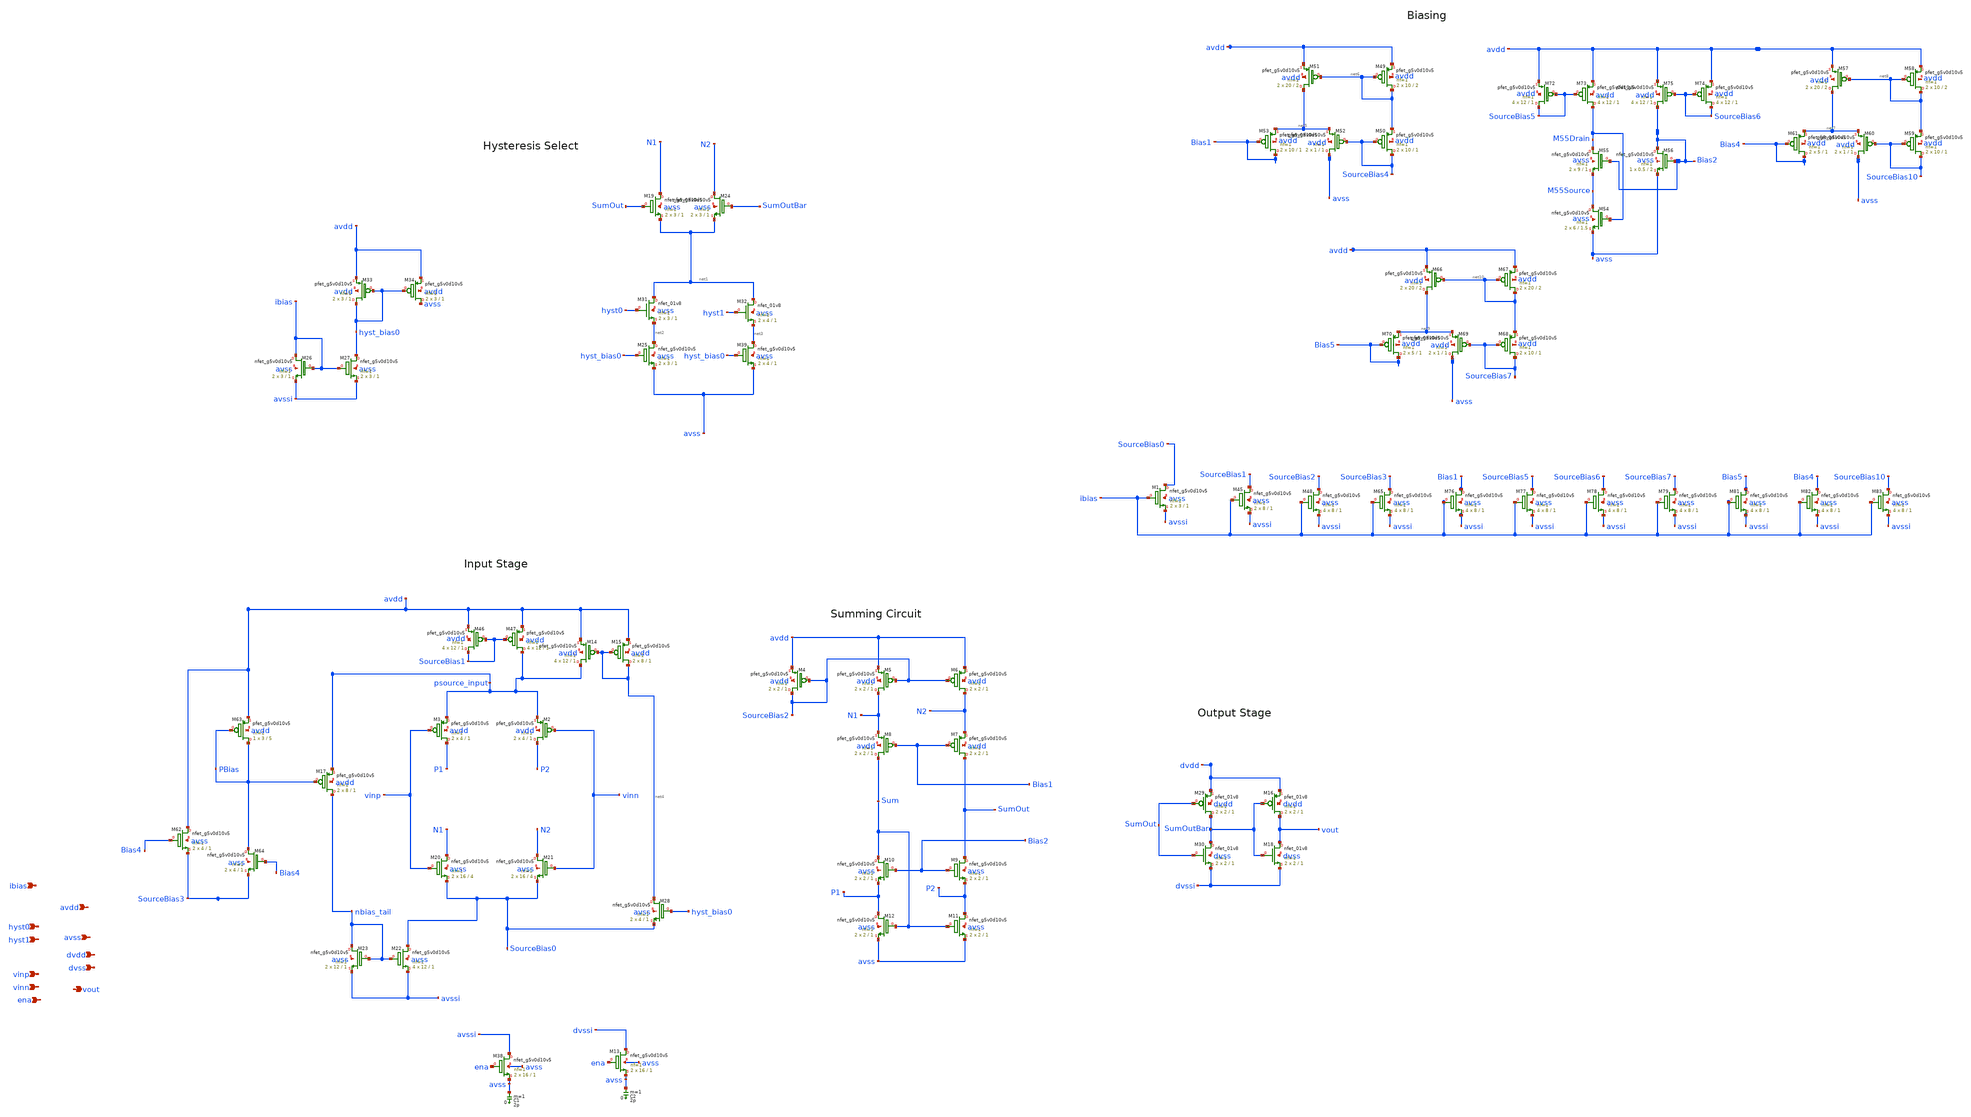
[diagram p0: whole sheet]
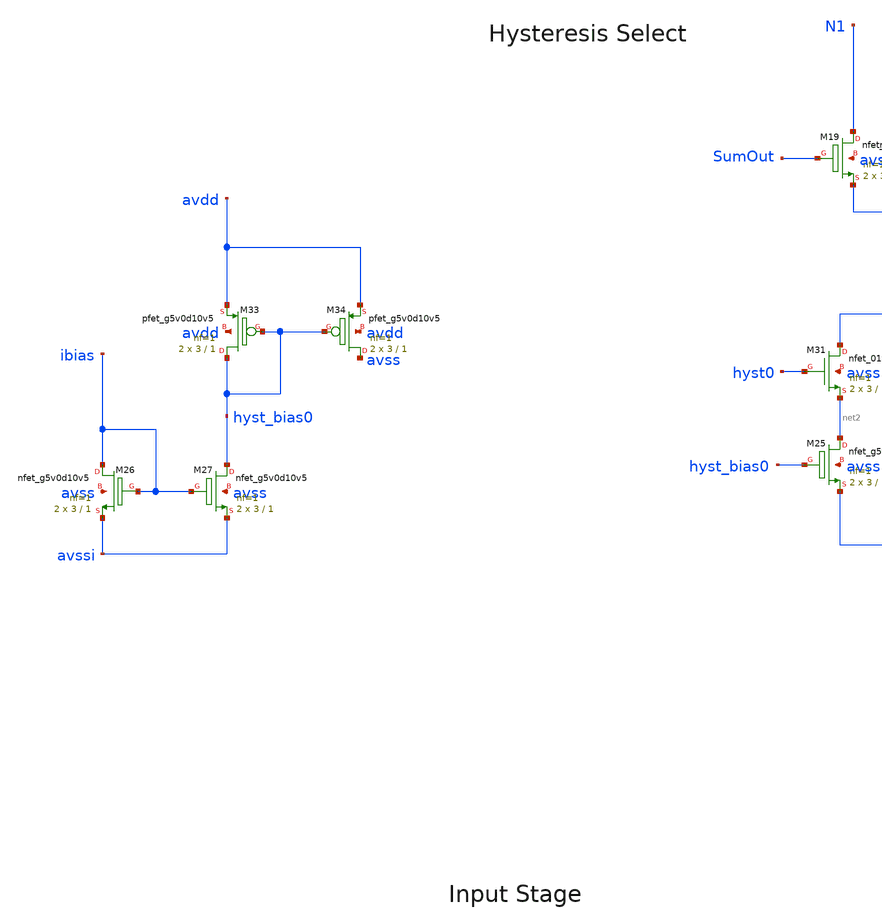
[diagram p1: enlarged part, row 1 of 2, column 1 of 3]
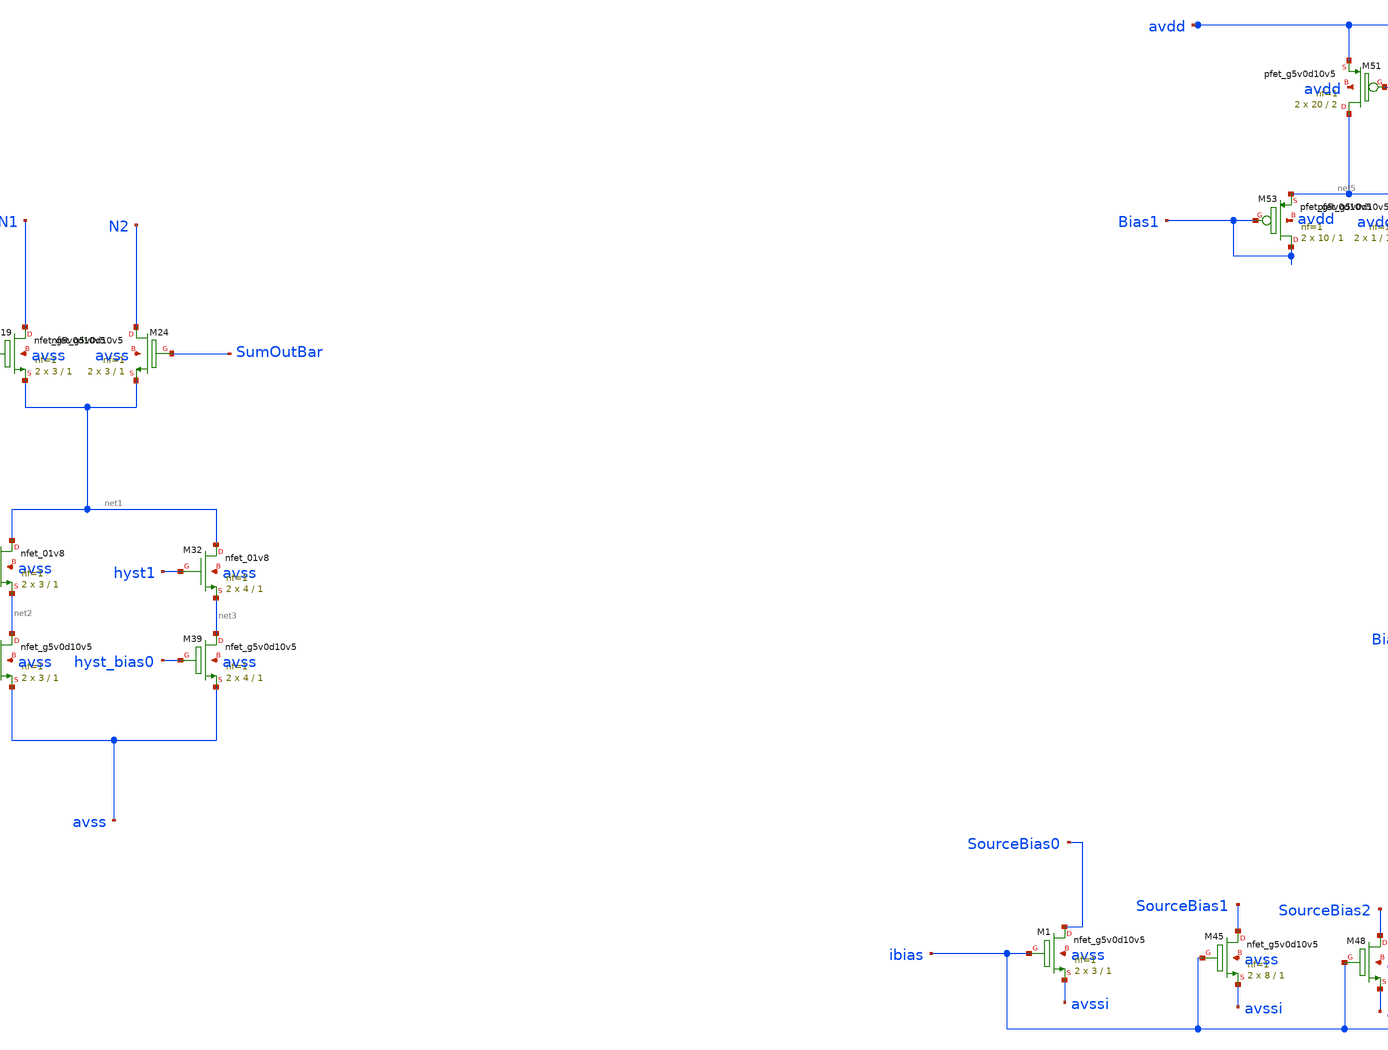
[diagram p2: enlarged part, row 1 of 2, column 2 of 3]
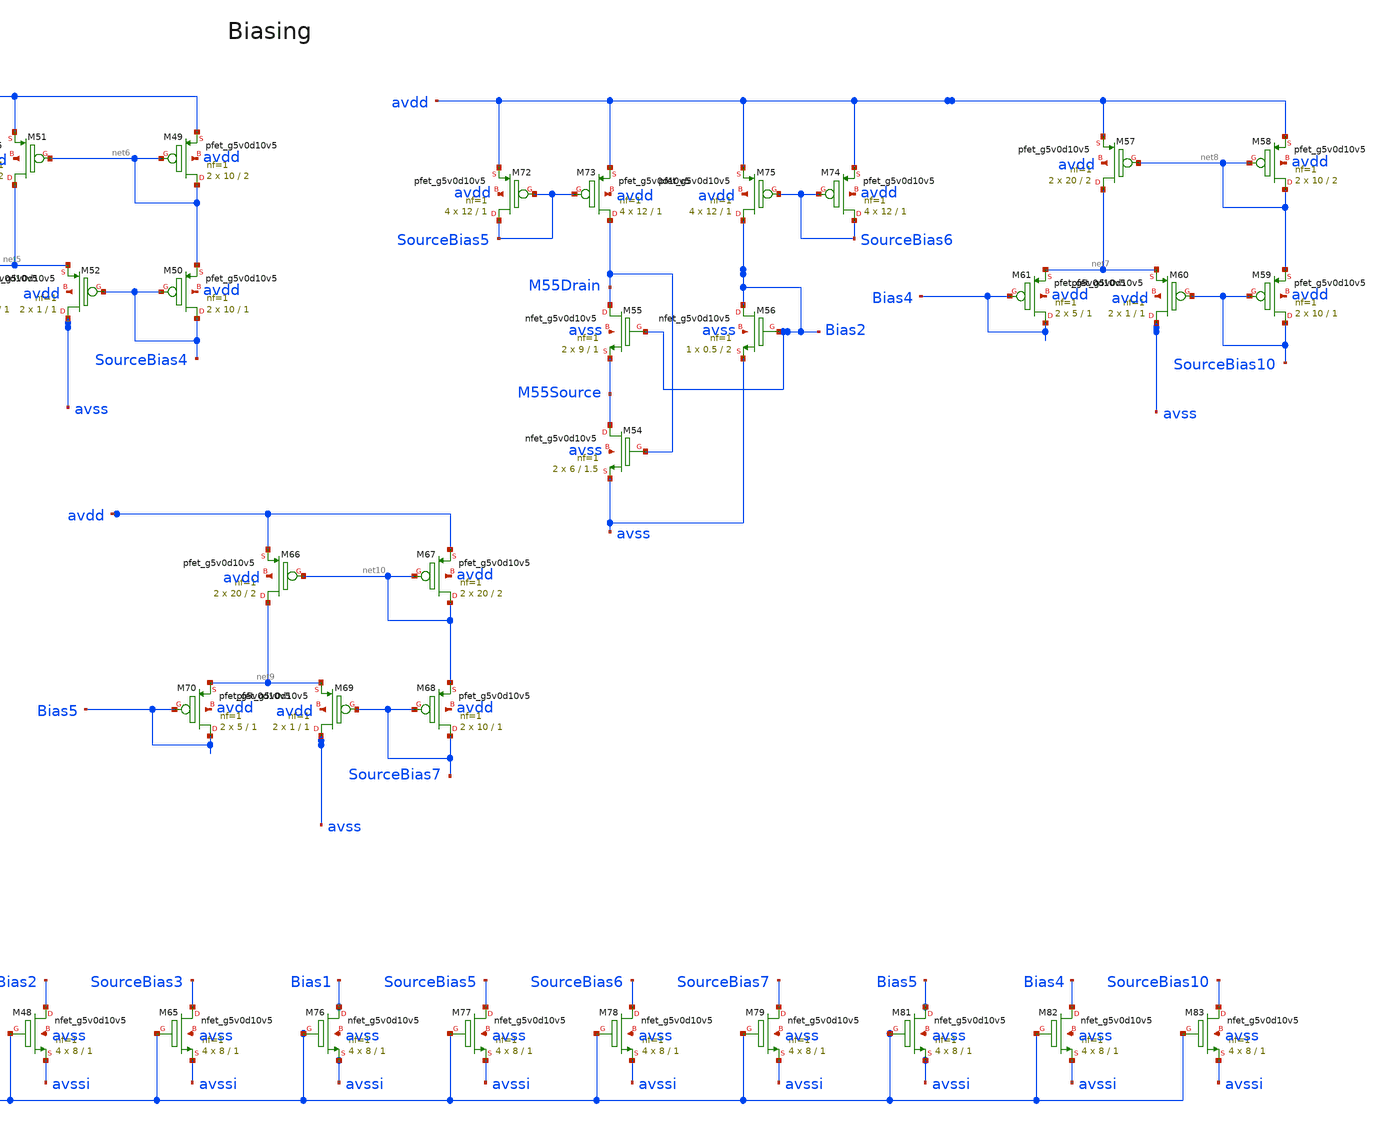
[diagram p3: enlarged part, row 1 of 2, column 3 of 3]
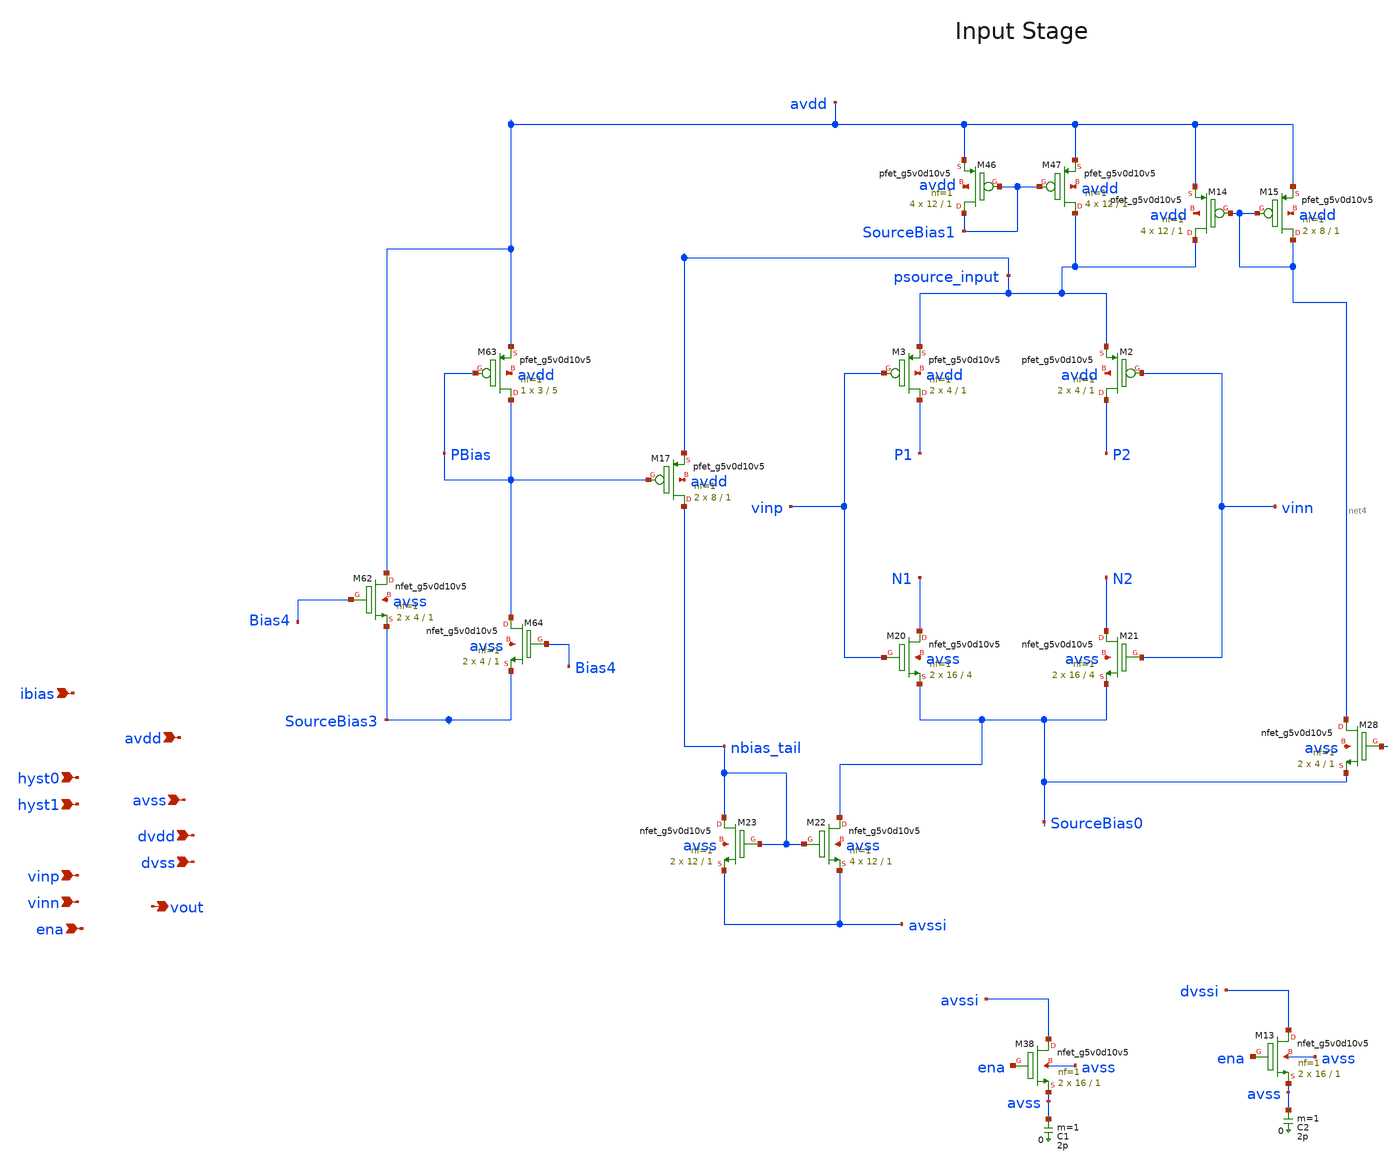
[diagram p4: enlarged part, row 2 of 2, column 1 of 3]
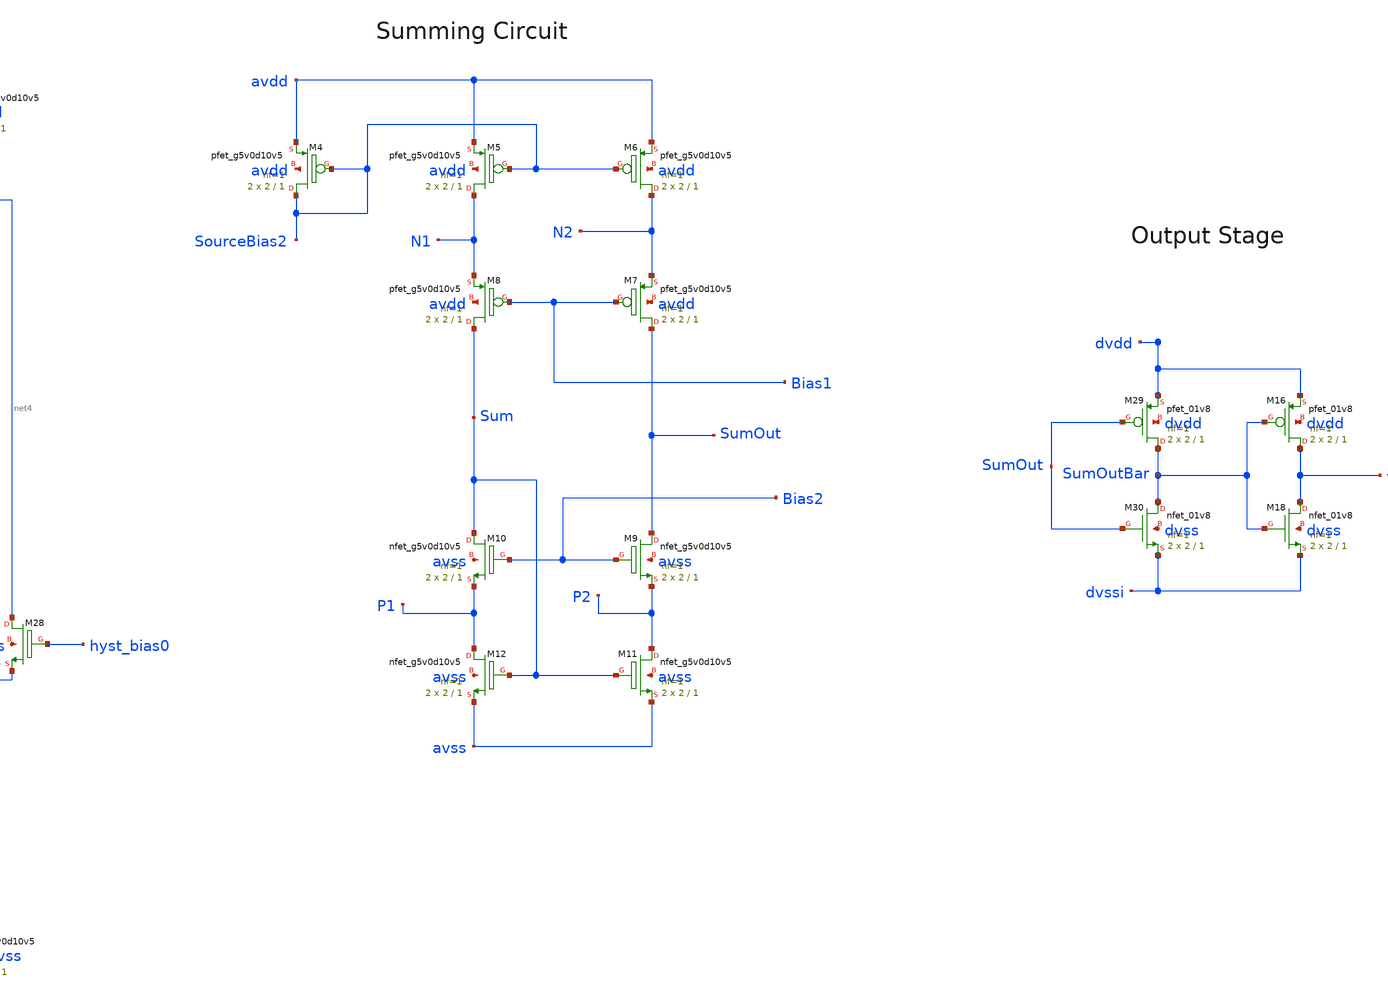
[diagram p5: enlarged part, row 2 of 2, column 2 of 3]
** sch_path: Chipalooza_April2024_Comparator/xschem/Chipalooza_April2024_Comparator.sch
**.subckt Chipalooza_April2024_Comparator vinp vinn hyst0 hyst1 avdd avss dvdd dvss vout ena ibias
*.ipin vinp
*.ipin vinn
*.ipin hyst0
*.ipin hyst1
*.ipin avdd
*.ipin avss
*.ipin dvdd
*.ipin dvss
*.opin vout
*.ipin ena
*.ipin ibias
XM29 SumOutBar SumOut dvdd dvdd sky130_fd_pr__pfet_01v8 L=1 W=2 nf=1 ad='int((nf+1)/2) * W/nf * 0.29'
+ as='int((nf+2)/2) * W/nf * 0.29' pd='2*int((nf+1)/2) * (W/nf + 0.29)' ps='2*int((nf+2)/2) * (W/nf + 0.29)'
+ nrd='0.29 / W' nrs='0.29 / W' sa=0 sb=0 sd=0 mult=2 m=2
XM30 SumOutBar SumOut dvssi dvss sky130_fd_pr__nfet_01v8 L=1 W=2 nf=1 ad='int((nf+1)/2) * W/nf * 0.29'
+ as='int((nf+2)/2) * W/nf * 0.29' pd='2*int((nf+1)/2) * (W/nf + 0.29)' ps='2*int((nf+2)/2) * (W/nf + 0.29)'
+ nrd='0.29 / W' nrs='0.29 / W' sa=0 sb=0 sd=0 mult=2 m=2
XM25 net2 hyst_bias0 avss avss sky130_fd_pr__nfet_g5v0d10v5 L=1 W=3 nf=1 ad='int((nf+1)/2) * W/nf * 0.29'
+ as='int((nf+2)/2) * W/nf * 0.29' pd='2*int((nf+1)/2) * (W/nf + 0.29)' ps='2*int((nf+2)/2) * (W/nf + 0.29)'
+ nrd='0.29 / W' nrs='0.29 / W' sa=0 sb=0 sd=0 mult=2 m=2
C1 avss 0 2p m=1
XM38 avssi ena avss avss sky130_fd_pr__nfet_g5v0d10v5 L=1 W=16 nf=1 ad='int((nf+1)/2) * W/nf * 0.29'
+ as='int((nf+2)/2) * W/nf * 0.29' pd='2*int((nf+1)/2) * (W/nf + 0.29)' ps='2*int((nf+2)/2) * (W/nf + 0.29)'
+ nrd='0.29 / W' nrs='0.29 / W' sa=0 sb=0 sd=0 mult=2 m=2
XM39 net3 hyst_bias0 avss avss sky130_fd_pr__nfet_g5v0d10v5 L=1 W=4 nf=1 ad='int((nf+1)/2) * W/nf * 0.29'
+ as='int((nf+2)/2) * W/nf * 0.29' pd='2*int((nf+1)/2) * (W/nf + 0.29)' ps='2*int((nf+2)/2) * (W/nf + 0.29)'
+ nrd='0.29 / W' nrs='0.29 / W' sa=0 sb=0 sd=0 mult=2 m=2
C2 avss 0 2p m=1
XM13 dvssi ena avss avss sky130_fd_pr__nfet_g5v0d10v5 L=1 W=16 nf=1 ad='int((nf+1)/2) * W/nf * 0.29'
+ as='int((nf+2)/2) * W/nf * 0.29' pd='2*int((nf+1)/2) * (W/nf + 0.29)' ps='2*int((nf+2)/2) * (W/nf + 0.29)'
+ nrd='0.29 / W' nrs='0.29 / W' sa=0 sb=0 sd=0 mult=2 m=2
XM16 vout SumOutBar dvdd dvdd sky130_fd_pr__pfet_01v8 L=1 W=2 nf=1 ad='int((nf+1)/2) * W/nf * 0.29' as='int((nf+2)/2) * W/nf * 0.29'
+ pd='2*int((nf+1)/2) * (W/nf + 0.29)' ps='2*int((nf+2)/2) * (W/nf + 0.29)' nrd='0.29 / W' nrs='0.29 / W'
+ sa=0 sb=0 sd=0 mult=2 m=2
XM18 vout SumOutBar dvssi dvss sky130_fd_pr__nfet_01v8 L=1 W=2 nf=1 ad='int((nf+1)/2) * W/nf * 0.29'
+ as='int((nf+2)/2) * W/nf * 0.29' pd='2*int((nf+1)/2) * (W/nf + 0.29)' ps='2*int((nf+2)/2) * (W/nf + 0.29)'
+ nrd='0.29 / W' nrs='0.29 / W' sa=0 sb=0 sd=0 mult=2 m=2
XM4 SourceBias2 SourceBias2 avdd avdd sky130_fd_pr__pfet_g5v0d10v5 L=1 W=2 nf=1 ad='int((nf+1)/2) * W/nf * 0.29'
+ as='int((nf+2)/2) * W/nf * 0.29' pd='2*int((nf+1)/2) * (W/nf + 0.29)' ps='2*int((nf+2)/2) * (W/nf + 0.29)'
+ nrd='0.29 / W' nrs='0.29 / W' sa=0 sb=0 sd=0 mult=2 m=2
XM5 N1 SourceBias2 avdd avdd sky130_fd_pr__pfet_g5v0d10v5 L=1 W=2 nf=1 ad='int((nf+1)/2) * W/nf * 0.29'
+ as='int((nf+2)/2) * W/nf * 0.29' pd='2*int((nf+1)/2) * (W/nf + 0.29)' ps='2*int((nf+2)/2) * (W/nf + 0.29)'
+ nrd='0.29 / W' nrs='0.29 / W' sa=0 sb=0 sd=0 mult=2 m=2
XM6 N2 SourceBias2 avdd avdd sky130_fd_pr__pfet_g5v0d10v5 L=1 W=2 nf=1 ad='int((nf+1)/2) * W/nf * 0.29'
+ as='int((nf+2)/2) * W/nf * 0.29' pd='2*int((nf+1)/2) * (W/nf + 0.29)' ps='2*int((nf+2)/2) * (W/nf + 0.29)'
+ nrd='0.29 / W' nrs='0.29 / W' sa=0 sb=0 sd=0 mult=2 m=2
XM7 SumOut Bias1 N2 avdd sky130_fd_pr__pfet_g5v0d10v5 L=1 W=2 nf=1 ad='int((nf+1)/2) * W/nf * 0.29' as='int((nf+2)/2) * W/nf * 0.29'
+ pd='2*int((nf+1)/2) * (W/nf + 0.29)' ps='2*int((nf+2)/2) * (W/nf + 0.29)' nrd='0.29 / W' nrs='0.29 / W'
+ sa=0 sb=0 sd=0 mult=2 m=2
XM8 Sum Bias1 N1 avdd sky130_fd_pr__pfet_g5v0d10v5 L=1 W=2 nf=1 ad='int((nf+1)/2) * W/nf * 0.29' as='int((nf+2)/2) * W/nf * 0.29'
+ pd='2*int((nf+1)/2) * (W/nf + 0.29)' ps='2*int((nf+2)/2) * (W/nf + 0.29)' nrd='0.29 / W' nrs='0.29 / W'
+ sa=0 sb=0 sd=0 mult=2 m=2
XM9 SumOut Bias2 P2 avss sky130_fd_pr__nfet_g5v0d10v5 L=1 W=2 nf=1 ad='int((nf+1)/2) * W/nf * 0.29' as='int((nf+2)/2) * W/nf * 0.29'
+ pd='2*int((nf+1)/2) * (W/nf + 0.29)' ps='2*int((nf+2)/2) * (W/nf + 0.29)' nrd='0.29 / W' nrs='0.29 / W'
+ sa=0 sb=0 sd=0 mult=2 m=2
XM10 Sum Bias2 P1 avss sky130_fd_pr__nfet_g5v0d10v5 L=1 W=2 nf=1 ad='int((nf+1)/2) * W/nf * 0.29' as='int((nf+2)/2) * W/nf * 0.29'
+ pd='2*int((nf+1)/2) * (W/nf + 0.29)' ps='2*int((nf+2)/2) * (W/nf + 0.29)' nrd='0.29 / W' nrs='0.29 / W'
+ sa=0 sb=0 sd=0 mult=2 m=2
XM11 P2 Sum avss avss sky130_fd_pr__nfet_g5v0d10v5 L=1 W=2 nf=1 ad='int((nf+1)/2) * W/nf * 0.29' as='int((nf+2)/2) * W/nf * 0.29'
+ pd='2*int((nf+1)/2) * (W/nf + 0.29)' ps='2*int((nf+2)/2) * (W/nf + 0.29)' nrd='0.29 / W' nrs='0.29 / W'
+ sa=0 sb=0 sd=0 mult=2 m=2
XM12 P1 Sum avss avss sky130_fd_pr__nfet_g5v0d10v5 L=1 W=2 nf=1 ad='int((nf+1)/2) * W/nf * 0.29' as='int((nf+2)/2) * W/nf * 0.29'
+ pd='2*int((nf+1)/2) * (W/nf + 0.29)' ps='2*int((nf+2)/2) * (W/nf + 0.29)' nrd='0.29 / W' nrs='0.29 / W'
+ sa=0 sb=0 sd=0 mult=2 m=2
XM2 P2 vinn psource_input avdd sky130_fd_pr__pfet_g5v0d10v5 L=1 W=4 nf=1 ad='int((nf+1)/2) * W/nf * 0.29'
+ as='int((nf+2)/2) * W/nf * 0.29' pd='2*int((nf+1)/2) * (W/nf + 0.29)' ps='2*int((nf+2)/2) * (W/nf + 0.29)'
+ nrd='0.29 / W' nrs='0.29 / W' sa=0 sb=0 sd=0 mult=2 m=2
XM3 P1 vinp psource_input avdd sky130_fd_pr__pfet_g5v0d10v5 L=1 W=4 nf=1 ad='int((nf+1)/2) * W/nf * 0.29'
+ as='int((nf+2)/2) * W/nf * 0.29' pd='2*int((nf+1)/2) * (W/nf + 0.29)' ps='2*int((nf+2)/2) * (W/nf + 0.29)'
+ nrd='0.29 / W' nrs='0.29 / W' sa=0 sb=0 sd=0 mult=2 m=2
XM14 psource_input net4 avdd avdd sky130_fd_pr__pfet_g5v0d10v5 L=1 W=12 nf=1 ad='int((nf+1)/2) * W/nf * 0.29'
+ as='int((nf+2)/2) * W/nf * 0.29' pd='2*int((nf+1)/2) * (W/nf + 0.29)' ps='2*int((nf+2)/2) * (W/nf + 0.29)'
+ nrd='0.29 / W' nrs='0.29 / W' sa=0 sb=0 sd=0 mult=4 m=4
XM15 net4 net4 avdd avdd sky130_fd_pr__pfet_g5v0d10v5 L=1 W=8 nf=1 ad='int((nf+1)/2) * W/nf * 0.29' as='int((nf+2)/2) * W/nf * 0.29'
+ pd='2*int((nf+1)/2) * (W/nf + 0.29)' ps='2*int((nf+2)/2) * (W/nf + 0.29)' nrd='0.29 / W' nrs='0.29 / W'
+ sa=0 sb=0 sd=0 mult=2 m=2
XM17 nbias_tail PBias psource_input avdd sky130_fd_pr__pfet_g5v0d10v5 L=1 W=8 nf=1 ad='int((nf+1)/2) * W/nf * 0.29'
+ as='int((nf+2)/2) * W/nf * 0.29' pd='2*int((nf+1)/2) * (W/nf + 0.29)' ps='2*int((nf+2)/2) * (W/nf + 0.29)'
+ nrd='0.29 / W' nrs='0.29 / W' sa=0 sb=0 sd=0 mult=2 m=2
XM20 N1 vinp SourceBias0 avss sky130_fd_pr__nfet_g5v0d10v5 L=4 W=16 nf=1 ad='int((nf+1)/2) * W/nf * 0.29'
+ as='int((nf+2)/2) * W/nf * 0.29' pd='2*int((nf+1)/2) * (W/nf + 0.29)' ps='2*int((nf+2)/2) * (W/nf + 0.29)'
+ nrd='0.29 / W' nrs='0.29 / W' sa=0 sb=0 sd=0 mult=2 m=2
XM21 N2 vinn SourceBias0 avss sky130_fd_pr__nfet_g5v0d10v5 L=4 W=16 nf=1 ad='int((nf+1)/2) * W/nf * 0.29'
+ as='int((nf+2)/2) * W/nf * 0.29' pd='2*int((nf+1)/2) * (W/nf + 0.29)' ps='2*int((nf+2)/2) * (W/nf + 0.29)'
+ nrd='0.29 / W' nrs='0.29 / W' sa=0 sb=0 sd=0 mult=2 m=2
XM22 SourceBias0 nbias_tail avssi avss sky130_fd_pr__nfet_g5v0d10v5 L=1 W=12 nf=1 ad='int((nf+1)/2) * W/nf * 0.29'
+ as='int((nf+2)/2) * W/nf * 0.29' pd='2*int((nf+1)/2) * (W/nf + 0.29)' ps='2*int((nf+2)/2) * (W/nf + 0.29)'
+ nrd='0.29 / W' nrs='0.29 / W' sa=0 sb=0 sd=0 mult=4 m=4
XM23 nbias_tail nbias_tail avssi avss sky130_fd_pr__nfet_g5v0d10v5 L=1 W=12 nf=1 ad='int((nf+1)/2) * W/nf * 0.29'
+ as='int((nf+2)/2) * W/nf * 0.29' pd='2*int((nf+1)/2) * (W/nf + 0.29)' ps='2*int((nf+2)/2) * (W/nf + 0.29)'
+ nrd='0.29 / W' nrs='0.29 / W' sa=0 sb=0 sd=0 mult=2 m=2
XM28 net4 hyst_bias0 SourceBias0 avss sky130_fd_pr__nfet_g5v0d10v5 L=1 W=4 nf=1 ad='int((nf+1)/2) * W/nf * 0.29'
+ as='int((nf+2)/2) * W/nf * 0.29' pd='2*int((nf+1)/2) * (W/nf + 0.29)' ps='2*int((nf+2)/2) * (W/nf + 0.29)'
+ nrd='0.29 / W' nrs='0.29 / W' sa=0 sb=0 sd=0 mult=2 m=2
XM45 SourceBias1 ibias avssi avss sky130_fd_pr__nfet_g5v0d10v5 L=1 W=8 nf=1 ad='int((nf+1)/2) * W/nf * 0.29'
+ as='int((nf+2)/2) * W/nf * 0.29' pd='2*int((nf+1)/2) * (W/nf + 0.29)' ps='2*int((nf+2)/2) * (W/nf + 0.29)'
+ nrd='0.29 / W' nrs='0.29 / W' sa=0 sb=0 sd=0 mult=2 m=2
XM46 SourceBias1 SourceBias1 avdd avdd sky130_fd_pr__pfet_g5v0d10v5 L=1 W=12 nf=1 ad='int((nf+1)/2) * W/nf * 0.29'
+ as='int((nf+2)/2) * W/nf * 0.29' pd='2*int((nf+1)/2) * (W/nf + 0.29)' ps='2*int((nf+2)/2) * (W/nf + 0.29)'
+ nrd='0.29 / W' nrs='0.29 / W' sa=0 sb=0 sd=0 mult=4 m=4
XM47 psource_input SourceBias1 avdd avdd sky130_fd_pr__pfet_g5v0d10v5 L=1 W=12 nf=1 ad='int((nf+1)/2) * W/nf * 0.29'
+ as='int((nf+2)/2) * W/nf * 0.29' pd='2*int((nf+1)/2) * (W/nf + 0.29)' ps='2*int((nf+2)/2) * (W/nf + 0.29)'
+ nrd='0.29 / W' nrs='0.29 / W' sa=0 sb=0 sd=0 mult=4 m=4
XM48 SourceBias2 ibias avssi avss sky130_fd_pr__nfet_g5v0d10v5 L=1 W=8 nf=1 ad='int((nf+1)/2) * W/nf * 0.29'
+ as='int((nf+2)/2) * W/nf * 0.29' pd='2*int((nf+1)/2) * (W/nf + 0.29)' ps='2*int((nf+2)/2) * (W/nf + 0.29)'
+ nrd='0.29 / W' nrs='0.29 / W' sa=0 sb=0 sd=0 mult=4 m=4
XM63 PBias PBias avdd avdd sky130_fd_pr__pfet_g5v0d10v5 L=5 W=3 nf=1 ad='int((nf+1)/2) * W/nf * 0.29'
+ as='int((nf+2)/2) * W/nf * 0.29' pd='2*int((nf+1)/2) * (W/nf + 0.29)' ps='2*int((nf+2)/2) * (W/nf + 0.29)'
+ nrd='0.29 / W' nrs='0.29 / W' sa=0 sb=0 sd=0 mult=1 m=1
XM62 avdd Bias4 SourceBias3 avss sky130_fd_pr__nfet_g5v0d10v5 L=1 W=4 nf=1 ad='int((nf+1)/2) * W/nf * 0.29'
+ as='int((nf+2)/2) * W/nf * 0.29' pd='2*int((nf+1)/2) * (W/nf + 0.29)' ps='2*int((nf+2)/2) * (W/nf + 0.29)'
+ nrd='0.29 / W' nrs='0.29 / W' sa=0 sb=0 sd=0 mult=2 m=2
XM64 PBias Bias4 SourceBias3 avss sky130_fd_pr__nfet_g5v0d10v5 L=1 W=4 nf=1 ad='int((nf+1)/2) * W/nf * 0.29'
+ as='int((nf+2)/2) * W/nf * 0.29' pd='2*int((nf+1)/2) * (W/nf + 0.29)' ps='2*int((nf+2)/2) * (W/nf + 0.29)'
+ nrd='0.29 / W' nrs='0.29 / W' sa=0 sb=0 sd=0 mult=2 m=2
XM65 SourceBias3 ibias avssi avss sky130_fd_pr__nfet_g5v0d10v5 L=1 W=8 nf=1 ad='int((nf+1)/2) * W/nf * 0.29'
+ as='int((nf+2)/2) * W/nf * 0.29' pd='2*int((nf+1)/2) * (W/nf + 0.29)' ps='2*int((nf+2)/2) * (W/nf + 0.29)'
+ nrd='0.29 / W' nrs='0.29 / W' sa=0 sb=0 sd=0 mult=4 m=4
XM76 Bias1 ibias avssi avss sky130_fd_pr__nfet_g5v0d10v5 L=1 W=8 nf=1 ad='int((nf+1)/2) * W/nf * 0.29'
+ as='int((nf+2)/2) * W/nf * 0.29' pd='2*int((nf+1)/2) * (W/nf + 0.29)' ps='2*int((nf+2)/2) * (W/nf + 0.29)'
+ nrd='0.29 / W' nrs='0.29 / W' sa=0 sb=0 sd=0 mult=4 m=4
XM77 SourceBias5 ibias avssi avss sky130_fd_pr__nfet_g5v0d10v5 L=1 W=8 nf=1 ad='int((nf+1)/2) * W/nf * 0.29'
+ as='int((nf+2)/2) * W/nf * 0.29' pd='2*int((nf+1)/2) * (W/nf + 0.29)' ps='2*int((nf+2)/2) * (W/nf + 0.29)'
+ nrd='0.29 / W' nrs='0.29 / W' sa=0 sb=0 sd=0 mult=4 m=4
XM78 SourceBias6 ibias avssi avss sky130_fd_pr__nfet_g5v0d10v5 L=1 W=8 nf=1 ad='int((nf+1)/2) * W/nf * 0.29'
+ as='int((nf+2)/2) * W/nf * 0.29' pd='2*int((nf+1)/2) * (W/nf + 0.29)' ps='2*int((nf+2)/2) * (W/nf + 0.29)'
+ nrd='0.29 / W' nrs='0.29 / W' sa=0 sb=0 sd=0 mult=4 m=4
XM79 SourceBias7 ibias avssi avss sky130_fd_pr__nfet_g5v0d10v5 L=1 W=8 nf=1 ad='int((nf+1)/2) * W/nf * 0.29'
+ as='int((nf+2)/2) * W/nf * 0.29' pd='2*int((nf+1)/2) * (W/nf + 0.29)' ps='2*int((nf+2)/2) * (W/nf + 0.29)'
+ nrd='0.29 / W' nrs='0.29 / W' sa=0 sb=0 sd=0 mult=4 m=4
XM81 Bias5 ibias avssi avss sky130_fd_pr__nfet_g5v0d10v5 L=1 W=8 nf=1 ad='int((nf+1)/2) * W/nf * 0.29'
+ as='int((nf+2)/2) * W/nf * 0.29' pd='2*int((nf+1)/2) * (W/nf + 0.29)' ps='2*int((nf+2)/2) * (W/nf + 0.29)'
+ nrd='0.29 / W' nrs='0.29 / W' sa=0 sb=0 sd=0 mult=4 m=4
XM82 Bias4 ibias avssi avss sky130_fd_pr__nfet_g5v0d10v5 L=1 W=8 nf=1 ad='int((nf+1)/2) * W/nf * 0.29'
+ as='int((nf+2)/2) * W/nf * 0.29' pd='2*int((nf+1)/2) * (W/nf + 0.29)' ps='2*int((nf+2)/2) * (W/nf + 0.29)'
+ nrd='0.29 / W' nrs='0.29 / W' sa=0 sb=0 sd=0 mult=4 m=4
XM83 SourceBias10 ibias avssi avss sky130_fd_pr__nfet_g5v0d10v5 L=1 W=8 nf=1 ad='int((nf+1)/2) * W/nf * 0.29'
+ as='int((nf+2)/2) * W/nf * 0.29' pd='2*int((nf+1)/2) * (W/nf + 0.29)' ps='2*int((nf+2)/2) * (W/nf + 0.29)'
+ nrd='0.29 / W' nrs='0.29 / W' sa=0 sb=0 sd=0 mult=4 m=4
XM54 M55Source M55Drain avss avss sky130_fd_pr__nfet_g5v0d10v5 L=1.5 W=6 nf=1 ad='int((nf+1)/2) * W/nf * 0.29'
+ as='int((nf+2)/2) * W/nf * 0.29' pd='2*int((nf+1)/2) * (W/nf + 0.29)' ps='2*int((nf+2)/2) * (W/nf + 0.29)'
+ nrd='0.29 / W' nrs='0.29 / W' sa=0 sb=0 sd=0 mult=2 m=2
XM55 M55Drain Bias2 M55Source avss sky130_fd_pr__nfet_g5v0d10v5 L=1 W=9 nf=1 ad='int((nf+1)/2) * W/nf * 0.29'
+ as='int((nf+2)/2) * W/nf * 0.29' pd='2*int((nf+1)/2) * (W/nf + 0.29)' ps='2*int((nf+2)/2) * (W/nf + 0.29)'
+ nrd='0.29 / W' nrs='0.29 / W' sa=0 sb=0 sd=0 mult=2 m=2
XM56 Bias2 Bias2 avss avss sky130_fd_pr__nfet_g5v0d10v5 L=2 W=0.5 nf=1 ad='int((nf+1)/2) * W/nf * 0.29'
+ as='int((nf+2)/2) * W/nf * 0.29' pd='2*int((nf+1)/2) * (W/nf + 0.29)' ps='2*int((nf+2)/2) * (W/nf + 0.29)'
+ nrd='0.29 / W' nrs='0.29 / W' sa=0 sb=0 sd=0 mult=1 m=1
XM51 net5 net6 avdd avdd sky130_fd_pr__pfet_g5v0d10v5 L=2 W=20 nf=1 ad='int((nf+1)/2) * W/nf * 0.29'
+ as='int((nf+2)/2) * W/nf * 0.29' pd='2*int((nf+1)/2) * (W/nf + 0.29)' ps='2*int((nf+2)/2) * (W/nf + 0.29)'
+ nrd='0.29 / W' nrs='0.29 / W' sa=0 sb=0 sd=0 mult=2 m=2
XM49 net6 net6 avdd avdd sky130_fd_pr__pfet_g5v0d10v5 L=2 W=10 nf=1 ad='int((nf+1)/2) * W/nf * 0.29'
+ as='int((nf+2)/2) * W/nf * 0.29' pd='2*int((nf+1)/2) * (W/nf + 0.29)' ps='2*int((nf+2)/2) * (W/nf + 0.29)'
+ nrd='0.29 / W' nrs='0.29 / W' sa=0 sb=0 sd=0 mult=2 m=2
XM50 SourceBias4 SourceBias4 net6 avdd sky130_fd_pr__pfet_g5v0d10v5 L=1 W=10 nf=1 ad='int((nf+1)/2) * W/nf * 0.29'
+ as='int((nf+2)/2) * W/nf * 0.29' pd='2*int((nf+1)/2) * (W/nf + 0.29)' ps='2*int((nf+2)/2) * (W/nf + 0.29)'
+ nrd='0.29 / W' nrs='0.29 / W' sa=0 sb=0 sd=0 mult=2 m=2
XM52 avss SourceBias4 net5 avdd sky130_fd_pr__pfet_g5v0d10v5 L=1 W=1 nf=1 ad='int((nf+1)/2) * W/nf * 0.29'
+ as='int((nf+2)/2) * W/nf * 0.29' pd='2*int((nf+1)/2) * (W/nf + 0.29)' ps='2*int((nf+2)/2) * (W/nf + 0.29)'
+ nrd='0.29 / W' nrs='0.29 / W' sa=0 sb=0 sd=0 mult=2 m=2
XM53 Bias1 Bias1 net5 avdd sky130_fd_pr__pfet_g5v0d10v5 L=1 W=10 nf=1 ad='int((nf+1)/2) * W/nf * 0.29'
+ as='int((nf+2)/2) * W/nf * 0.29' pd='2*int((nf+1)/2) * (W/nf + 0.29)' ps='2*int((nf+2)/2) * (W/nf + 0.29)'
+ nrd='0.29 / W' nrs='0.29 / W' sa=0 sb=0 sd=0 mult=2 m=2
XM57 net7 net8 avdd avdd sky130_fd_pr__pfet_g5v0d10v5 L=2 W=20 nf=1 ad='int((nf+1)/2) * W/nf * 0.29'
+ as='int((nf+2)/2) * W/nf * 0.29' pd='2*int((nf+1)/2) * (W/nf + 0.29)' ps='2*int((nf+2)/2) * (W/nf + 0.29)'
+ nrd='0.29 / W' nrs='0.29 / W' sa=0 sb=0 sd=0 mult=2 m=2
XM58 net8 net8 avdd avdd sky130_fd_pr__pfet_g5v0d10v5 L=2 W=10 nf=1 ad='int((nf+1)/2) * W/nf * 0.29'
+ as='int((nf+2)/2) * W/nf * 0.29' pd='2*int((nf+1)/2) * (W/nf + 0.29)' ps='2*int((nf+2)/2) * (W/nf + 0.29)'
+ nrd='0.29 / W' nrs='0.29 / W' sa=0 sb=0 sd=0 mult=2 m=2
XM59 SourceBias10 SourceBias10 net8 avdd sky130_fd_pr__pfet_g5v0d10v5 L=1 W=10 nf=1 ad='int((nf+1)/2) * W/nf * 0.29'
+ as='int((nf+2)/2) * W/nf * 0.29' pd='2*int((nf+1)/2) * (W/nf + 0.29)' ps='2*int((nf+2)/2) * (W/nf + 0.29)'
+ nrd='0.29 / W' nrs='0.29 / W' sa=0 sb=0 sd=0 mult=2 m=2
XM60 avss SourceBias10 net7 avdd sky130_fd_pr__pfet_g5v0d10v5 L=1 W=1 nf=1 ad='int((nf+1)/2) * W/nf * 0.29'
+ as='int((nf+2)/2) * W/nf * 0.29' pd='2*int((nf+1)/2) * (W/nf + 0.29)' ps='2*int((nf+2)/2) * (W/nf + 0.29)'
+ nrd='0.29 / W' nrs='0.29 / W' sa=0 sb=0 sd=0 mult=2 m=2
XM61 Bias4 Bias4 net7 avdd sky130_fd_pr__pfet_g5v0d10v5 L=1 W=5 nf=1 ad='int((nf+1)/2) * W/nf * 0.29'
+ as='int((nf+2)/2) * W/nf * 0.29' pd='2*int((nf+1)/2) * (W/nf + 0.29)' ps='2*int((nf+2)/2) * (W/nf + 0.29)'
+ nrd='0.29 / W' nrs='0.29 / W' sa=0 sb=0 sd=0 mult=2 m=2
XM66 net9 net10 avdd avdd sky130_fd_pr__pfet_g5v0d10v5 L=2 W=20 nf=1 ad='int((nf+1)/2) * W/nf * 0.29'
+ as='int((nf+2)/2) * W/nf * 0.29' pd='2*int((nf+1)/2) * (W/nf + 0.29)' ps='2*int((nf+2)/2) * (W/nf + 0.29)'
+ nrd='0.29 / W' nrs='0.29 / W' sa=0 sb=0 sd=0 mult=2 m=2
XM67 net10 net10 avdd avdd sky130_fd_pr__pfet_g5v0d10v5 L=2 W=20 nf=1 ad='int((nf+1)/2) * W/nf * 0.29'
+ as='int((nf+2)/2) * W/nf * 0.29' pd='2*int((nf+1)/2) * (W/nf + 0.29)' ps='2*int((nf+2)/2) * (W/nf + 0.29)'
+ nrd='0.29 / W' nrs='0.29 / W' sa=0 sb=0 sd=0 mult=2 m=2
XM68 SourceBias7 SourceBias7 net10 avdd sky130_fd_pr__pfet_g5v0d10v5 L=1 W=10 nf=1 ad='int((nf+1)/2) * W/nf * 0.29'
+ as='int((nf+2)/2) * W/nf * 0.29' pd='2*int((nf+1)/2) * (W/nf + 0.29)' ps='2*int((nf+2)/2) * (W/nf + 0.29)'
+ nrd='0.29 / W' nrs='0.29 / W' sa=0 sb=0 sd=0 mult=2 m=2
XM69 avss SourceBias7 net9 avdd sky130_fd_pr__pfet_g5v0d10v5 L=1 W=1 nf=1 ad='int((nf+1)/2) * W/nf * 0.29'
+ as='int((nf+2)/2) * W/nf * 0.29' pd='2*int((nf+1)/2) * (W/nf + 0.29)' ps='2*int((nf+2)/2) * (W/nf + 0.29)'
+ nrd='0.29 / W' nrs='0.29 / W' sa=0 sb=0 sd=0 mult=2 m=2
XM70 Bias5 Bias5 net9 avdd sky130_fd_pr__pfet_g5v0d10v5 L=1 W=5 nf=1 ad='int((nf+1)/2) * W/nf * 0.29'
+ as='int((nf+2)/2) * W/nf * 0.29' pd='2*int((nf+1)/2) * (W/nf + 0.29)' ps='2*int((nf+2)/2) * (W/nf + 0.29)'
+ nrd='0.29 / W' nrs='0.29 / W' sa=0 sb=0 sd=0 mult=2 m=2
XM72 SourceBias5 SourceBias5 avdd avdd sky130_fd_pr__pfet_g5v0d10v5 L=1 W=12 nf=1 ad='int((nf+1)/2) * W/nf * 0.29'
+ as='int((nf+2)/2) * W/nf * 0.29' pd='2*int((nf+1)/2) * (W/nf + 0.29)' ps='2*int((nf+2)/2) * (W/nf + 0.29)'
+ nrd='0.29 / W' nrs='0.29 / W' sa=0 sb=0 sd=0 mult=4 m=4
XM73 M55Drain SourceBias5 avdd avdd sky130_fd_pr__pfet_g5v0d10v5 L=1 W=12 nf=1 ad='int((nf+1)/2) * W/nf * 0.29'
+ as='int((nf+2)/2) * W/nf * 0.29' pd='2*int((nf+1)/2) * (W/nf + 0.29)' ps='2*int((nf+2)/2) * (W/nf + 0.29)'
+ nrd='0.29 / W' nrs='0.29 / W' sa=0 sb=0 sd=0 mult=4 m=4
XM74 SourceBias6 SourceBias6 avdd avdd sky130_fd_pr__pfet_g5v0d10v5 L=1 W=12 nf=1 ad='int((nf+1)/2) * W/nf * 0.29'
+ as='int((nf+2)/2) * W/nf * 0.29' pd='2*int((nf+1)/2) * (W/nf + 0.29)' ps='2*int((nf+2)/2) * (W/nf + 0.29)'
+ nrd='0.29 / W' nrs='0.29 / W' sa=0 sb=0 sd=0 mult=4 m=4
XM75 Bias2 SourceBias6 avdd avdd sky130_fd_pr__pfet_g5v0d10v5 L=1 W=12 nf=1 ad='int((nf+1)/2) * W/nf * 0.29'
+ as='int((nf+2)/2) * W/nf * 0.29' pd='2*int((nf+1)/2) * (W/nf + 0.29)' ps='2*int((nf+2)/2) * (W/nf + 0.29)'
+ nrd='0.29 / W' nrs='0.29 / W' sa=0 sb=0 sd=0 mult=4 m=4
XM1 SourceBias0 ibias avssi avss sky130_fd_pr__nfet_g5v0d10v5 L=1 W=3 nf=1 ad='int((nf+1)/2) * W/nf * 0.29'
+ as='int((nf+2)/2) * W/nf * 0.29' pd='2*int((nf+1)/2) * (W/nf + 0.29)' ps='2*int((nf+2)/2) * (W/nf + 0.29)'
+ nrd='0.29 / W' nrs='0.29 / W' sa=0 sb=0 sd=0 mult=2 m=2
XM31 net1 hyst0 net2 avss sky130_fd_pr__nfet_01v8 L=1 W=3 nf=1 ad='int((1 + 1)/2) * 3 / 1 * 0.29' as='int((1 + 2)/2) * 3 / 1 * 0.29'
+ pd='2*int((1 + 1)/2) * (3 / 1 + 0.29)' ps='2*int((1 + 2)/2) * (3 / 1 + 0.29)' nrd='0.29 / 3 ' nrs='0.29 / 3 '
+ sa=0 sb=0 sd=0 mult=2 m=2
XM32 net1 hyst1 net3 avss sky130_fd_pr__nfet_01v8 L=1 W=4 nf=1 ad='int((1 + 1)/2) * 4 / 1 * 0.29' as='int((1 + 2)/2) * 4 / 1 * 0.29'
+ pd='2*int((1 + 1)/2) * (4 / 1 + 0.29)' ps='2*int((1 + 2)/2) * (4 / 1 + 0.29)' nrd='0.29 / 4 ' nrs='0.29 / 4 '
+ sa=0 sb=0 sd=0 mult=2 m=2
XM19 N1 SumOut net1 avss sky130_fd_pr__nfet_g5v0d10v5 L=1 W=3 nf=1 ad='int((nf+1)/2) * W/nf * 0.29' as='int((nf+2)/2) * W/nf * 0.29'
+ pd='2*int((nf+1)/2) * (W/nf + 0.29)' ps='2*int((nf+2)/2) * (W/nf + 0.29)' nrd='0.29 / W' nrs='0.29 / W'
+ sa=0 sb=0 sd=0 mult=2 m=2
XM24 N2 SumOutBar net1 avss sky130_fd_pr__nfet_g5v0d10v5 L=1 W=3 nf=1 ad='int((nf+1)/2) * W/nf * 0.29'
+ as='int((nf+2)/2) * W/nf * 0.29' pd='2*int((nf+1)/2) * (W/nf + 0.29)' ps='2*int((nf+2)/2) * (W/nf + 0.29)'
+ nrd='0.29 / W' nrs='0.29 / W' sa=0 sb=0 sd=0 mult=2 m=2
XM26 ibias ibias avssi avss sky130_fd_pr__nfet_g5v0d10v5 L=1 W=3 nf=1 ad='int((nf+1)/2) * W/nf * 0.29'
+ as='int((nf+2)/2) * W/nf * 0.29' pd='2*int((nf+1)/2) * (W/nf + 0.29)' ps='2*int((nf+2)/2) * (W/nf + 0.29)'
+ nrd='0.29 / W' nrs='0.29 / W' sa=0 sb=0 sd=0 mult=2 m=2
XM27 hyst_bias0 ibias avssi avss sky130_fd_pr__nfet_g5v0d10v5 L=1 W=3 nf=1 ad='int((nf+1)/2) * W/nf * 0.29'
+ as='int((nf+2)/2) * W/nf * 0.29' pd='2*int((nf+1)/2) * (W/nf + 0.29)' ps='2*int((nf+2)/2) * (W/nf + 0.29)'
+ nrd='0.29 / W' nrs='0.29 / W' sa=0 sb=0 sd=0 mult=2 m=2
XM33 hyst_bias0 hyst_bias0 avdd avdd sky130_fd_pr__pfet_g5v0d10v5 L=1 W=3 nf=1 ad='int((nf+1)/2) * W/nf * 0.29'
+ as='int((nf+2)/2) * W/nf * 0.29' pd='2*int((nf+1)/2) * (W/nf + 0.29)' ps='2*int((nf+2)/2) * (W/nf + 0.29)'
+ nrd='0.29 / W' nrs='0.29 / W' sa=0 sb=0 sd=0 mult=2 m=2
XM34 avss hyst_bias0 avdd avdd sky130_fd_pr__pfet_g5v0d10v5 L=1 W=3 nf=1 ad='int((nf+1)/2) * W/nf * 0.29'
+ as='int((nf+2)/2) * W/nf * 0.29' pd='2*int((nf+1)/2) * (W/nf + 0.29)' ps='2*int((nf+2)/2) * (W/nf + 0.29)'
+ nrd='0.29 / W' nrs='0.29 / W' sa=0 sb=0 sd=0 mult=2 m=2
**.ends
.end
